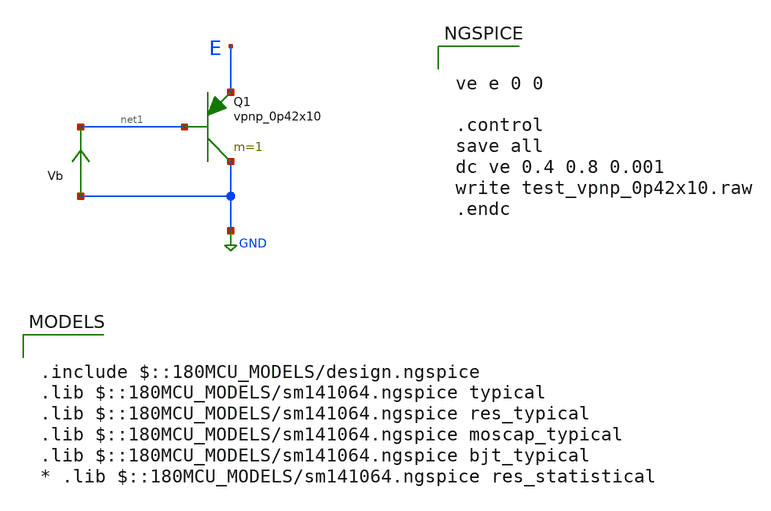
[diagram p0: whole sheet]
** sch_path: cells/xschem/tests/test_vpnp_0p42x10.sch
* Copyright 2022 GlobalFoundries PDK Authors
* Licensed under the Apache License, Version 2.0 (the "License");
* you may not use this file except in compliance with the License.
* You may obtain a copy of the License at
* https://www.apache.org/licenses/LICENSE-2.0
* Unless required by applicable law or agreed to in writing, software
* distributed under the License is distributed on an "AS IS" BASIS,
* WITHOUT WARRANTIES OR CONDITIONS OF ANY KIND, either express or implied.
* See the License for the specific language governing permissions and
* limitations under the License.
**.subckt test_vpnp_0p42x10
XQ1 GND net1 E vpnp_0p42x10 m=1
Vb GND net1 0
.save i(vb)
**** begin user architecture code

.include $::180MCU_MODELS/design.ngspice
.lib $::180MCU_MODELS/sm141064.ngspice typical
.lib $::180MCU_MODELS/sm141064.ngspice res_typical
.lib $::180MCU_MODELS/sm141064.ngspice moscap_typical
.lib $::180MCU_MODELS/sm141064.ngspice bjt_typical
* .lib $::180MCU_MODELS/sm141064.ngspice res_statistical



ve e 0 0

.control
save all
dc ve 0.4 0.8 0.001
write test_vpnp_0p42x10.raw
.endc


**** end user architecture code
**.ends
.GLOBAL GND
.end
